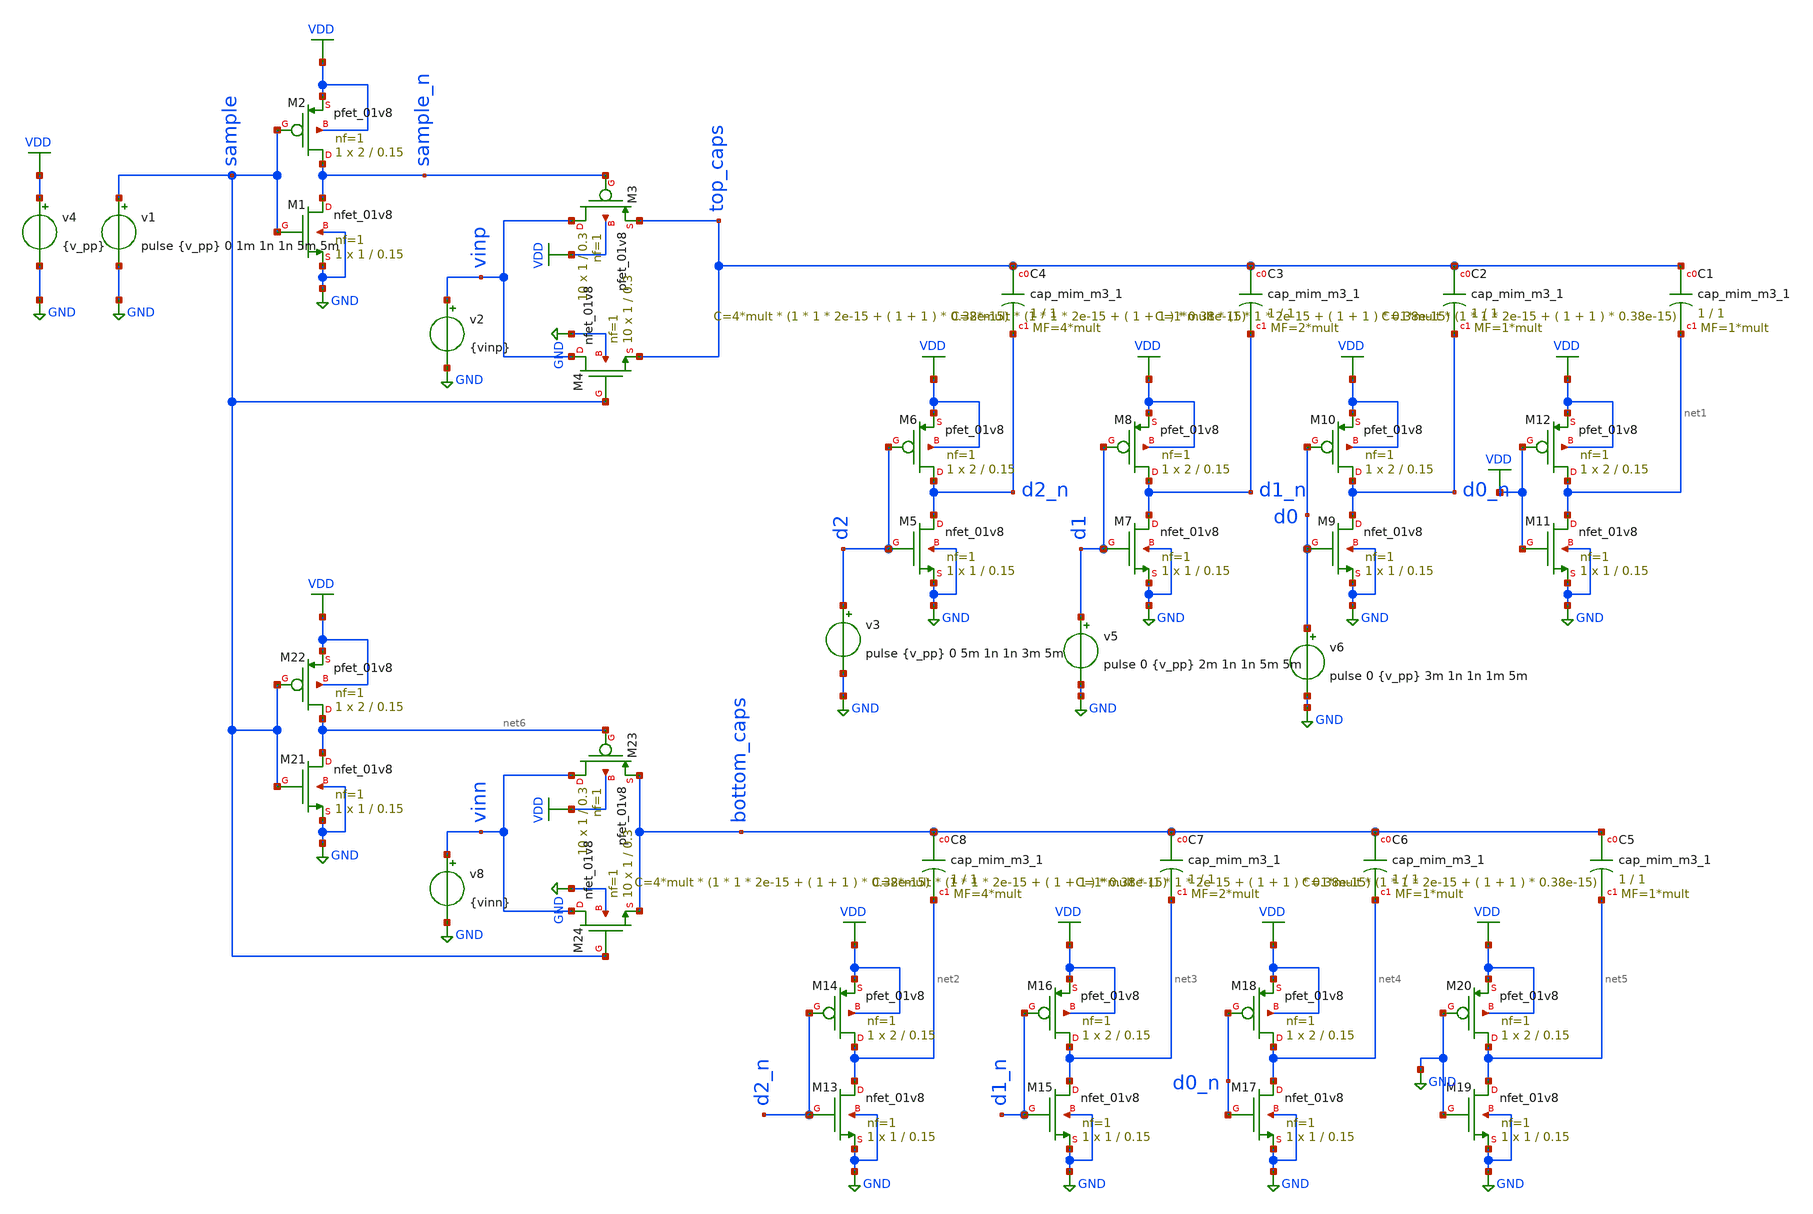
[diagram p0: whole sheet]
** sch_path: Schematics/ADC/simulations_adc_various/remake_c_transistors.sch
**.subckt remake_c_transistors
v1 sample GND pulse {v_pp} 0 1m 1n 1n 5m 5m
v4 VDD GND {v_pp}
XM1 sample_n sample GND GND sky130_fd_pr__nfet_01v8 L=0.15 W=1 nf=1 ad='int((nf+1)/2) * W/nf * 0.29'
+ as='int((nf+2)/2) * W/nf * 0.29' pd='2*int((nf+1)/2) * (W/nf + 0.29)' ps='2*int((nf+2)/2) * (W/nf + 0.29)'
+ nrd='0.29 / W' nrs='0.29 / W' sa=0 sb=0 sd=0 mult=1 m=1
XM2 sample_n sample VDD VDD sky130_fd_pr__pfet_01v8 L=0.15 W=2 nf=1 ad='int((nf+1)/2) * W/nf * 0.29'
+ as='int((nf+2)/2) * W/nf * 0.29' pd='2*int((nf+1)/2) * (W/nf + 0.29)' ps='2*int((nf+2)/2) * (W/nf + 0.29)'
+ nrd='0.29 / W' nrs='0.29 / W' sa=0 sb=0 sd=0 mult=1 m=1
XM3 vinp sample_n top_caps VDD sky130_fd_pr__pfet_01v8 L=0.3 W=1 nf=1 ad='int((nf+1)/2) * W/nf * 0.29'
+ as='int((nf+2)/2) * W/nf * 0.29' pd='2*int((nf+1)/2) * (W/nf + 0.29)' ps='2*int((nf+2)/2) * (W/nf + 0.29)'
+ nrd='0.29 / W' nrs='0.29 / W' sa=0 sb=0 sd=0 mult=10 m=10
XM4 vinp sample top_caps GND sky130_fd_pr__nfet_01v8 L=0.3 W=1 nf=1 ad='int((nf+1)/2) * W/nf * 0.29'
+ as='int((nf+2)/2) * W/nf * 0.29' pd='2*int((nf+1)/2) * (W/nf + 0.29)' ps='2*int((nf+2)/2) * (W/nf + 0.29)'
+ nrd='0.29 / W' nrs='0.29 / W' sa=0 sb=0 sd=0 mult=10 m=10
v2 vinp GND {vinp}
XM5 d2_n d2 GND GND sky130_fd_pr__nfet_01v8 L=0.15 W=1 nf=1 ad='int((nf+1)/2) * W/nf * 0.29' as='int((nf+2)/2) * W/nf * 0.29'
+ pd='2*int((nf+1)/2) * (W/nf + 0.29)' ps='2*int((nf+2)/2) * (W/nf + 0.29)' nrd='0.29 / W' nrs='0.29 / W'
+ sa=0 sb=0 sd=0 mult=1 m=1
XM6 d2_n d2 VDD VDD sky130_fd_pr__pfet_01v8 L=0.15 W=2 nf=1 ad='int((nf+1)/2) * W/nf * 0.29' as='int((nf+2)/2) * W/nf * 0.29'
+ pd='2*int((nf+1)/2) * (W/nf + 0.29)' ps='2*int((nf+2)/2) * (W/nf + 0.29)' nrd='0.29 / W' nrs='0.29 / W'
+ sa=0 sb=0 sd=0 mult=1 m=1
XM7 d1_n d1 GND GND sky130_fd_pr__nfet_01v8 L=0.15 W=1 nf=1 ad='int((nf+1)/2) * W/nf * 0.29' as='int((nf+2)/2) * W/nf * 0.29'
+ pd='2*int((nf+1)/2) * (W/nf + 0.29)' ps='2*int((nf+2)/2) * (W/nf + 0.29)' nrd='0.29 / W' nrs='0.29 / W'
+ sa=0 sb=0 sd=0 mult=1 m=1
XM8 d1_n d1 VDD VDD sky130_fd_pr__pfet_01v8 L=0.15 W=2 nf=1 ad='int((nf+1)/2) * W/nf * 0.29' as='int((nf+2)/2) * W/nf * 0.29'
+ pd='2*int((nf+1)/2) * (W/nf + 0.29)' ps='2*int((nf+2)/2) * (W/nf + 0.29)' nrd='0.29 / W' nrs='0.29 / W'
+ sa=0 sb=0 sd=0 mult=1 m=1
XM9 d0_n d0 GND GND sky130_fd_pr__nfet_01v8 L=0.15 W=1 nf=1 ad='int((nf+1)/2) * W/nf * 0.29' as='int((nf+2)/2) * W/nf * 0.29'
+ pd='2*int((nf+1)/2) * (W/nf + 0.29)' ps='2*int((nf+2)/2) * (W/nf + 0.29)' nrd='0.29 / W' nrs='0.29 / W'
+ sa=0 sb=0 sd=0 mult=1 m=1
XM10 d0_n d0 VDD VDD sky130_fd_pr__pfet_01v8 L=0.15 W=2 nf=1 ad='int((nf+1)/2) * W/nf * 0.29' as='int((nf+2)/2) * W/nf * 0.29'
+ pd='2*int((nf+1)/2) * (W/nf + 0.29)' ps='2*int((nf+2)/2) * (W/nf + 0.29)' nrd='0.29 / W' nrs='0.29 / W'
+ sa=0 sb=0 sd=0 mult=1 m=1
XM11 net1 VDD GND GND sky130_fd_pr__nfet_01v8 L=0.15 W=1 nf=1 ad='int((nf+1)/2) * W/nf * 0.29' as='int((nf+2)/2) * W/nf * 0.29'
+ pd='2*int((nf+1)/2) * (W/nf + 0.29)' ps='2*int((nf+2)/2) * (W/nf + 0.29)' nrd='0.29 / W' nrs='0.29 / W'
+ sa=0 sb=0 sd=0 mult=1 m=1
XM12 net1 VDD VDD VDD sky130_fd_pr__pfet_01v8 L=0.15 W=2 nf=1 ad='int((nf+1)/2) * W/nf * 0.29' as='int((nf+2)/2) * W/nf * 0.29'
+ pd='2*int((nf+1)/2) * (W/nf + 0.29)' ps='2*int((nf+2)/2) * (W/nf + 0.29)' nrd='0.29 / W' nrs='0.29 / W'
+ sa=0 sb=0 sd=0 mult=1 m=1
XC1 top_caps net1 sky130_fd_pr__cap_mim_m3_1 W=1 L=1 MF=1*mult m=1*mult
XC2 top_caps d0_n sky130_fd_pr__cap_mim_m3_1 W=1 L=1 MF=1*mult m=1*mult
XC3 top_caps d1_n sky130_fd_pr__cap_mim_m3_1 W=1 L=1 MF=2*mult m=2*mult
XC4 top_caps d2_n sky130_fd_pr__cap_mim_m3_1 W=1 L=1 MF=4*mult m=4*mult
v3 d2 GND pulse {v_pp} 0 5m 1n 1n 3m 5m
v5 d1 GND pulse 0 {v_pp} 2m 1n 1n 5m 5m
v6 d0 GND pulse 0 {v_pp} 3m 1n 1n 1m 5m
XM13 net2 d2_n GND GND sky130_fd_pr__nfet_01v8 L=0.15 W=1 nf=1 ad='int((nf+1)/2) * W/nf * 0.29' as='int((nf+2)/2) * W/nf * 0.29'
+ pd='2*int((nf+1)/2) * (W/nf + 0.29)' ps='2*int((nf+2)/2) * (W/nf + 0.29)' nrd='0.29 / W' nrs='0.29 / W'
+ sa=0 sb=0 sd=0 mult=1 m=1
XM14 net2 d2_n VDD VDD sky130_fd_pr__pfet_01v8 L=0.15 W=2 nf=1 ad='int((nf+1)/2) * W/nf * 0.29' as='int((nf+2)/2) * W/nf * 0.29'
+ pd='2*int((nf+1)/2) * (W/nf + 0.29)' ps='2*int((nf+2)/2) * (W/nf + 0.29)' nrd='0.29 / W' nrs='0.29 / W'
+ sa=0 sb=0 sd=0 mult=1 m=1
XM15 net3 d1_n GND GND sky130_fd_pr__nfet_01v8 L=0.15 W=1 nf=1 ad='int((nf+1)/2) * W/nf * 0.29' as='int((nf+2)/2) * W/nf * 0.29'
+ pd='2*int((nf+1)/2) * (W/nf + 0.29)' ps='2*int((nf+2)/2) * (W/nf + 0.29)' nrd='0.29 / W' nrs='0.29 / W'
+ sa=0 sb=0 sd=0 mult=1 m=1
XM16 net3 d1_n VDD VDD sky130_fd_pr__pfet_01v8 L=0.15 W=2 nf=1 ad='int((nf+1)/2) * W/nf * 0.29' as='int((nf+2)/2) * W/nf * 0.29'
+ pd='2*int((nf+1)/2) * (W/nf + 0.29)' ps='2*int((nf+2)/2) * (W/nf + 0.29)' nrd='0.29 / W' nrs='0.29 / W'
+ sa=0 sb=0 sd=0 mult=1 m=1
XM17 net4 d0_n GND GND sky130_fd_pr__nfet_01v8 L=0.15 W=1 nf=1 ad='int((nf+1)/2) * W/nf * 0.29' as='int((nf+2)/2) * W/nf * 0.29'
+ pd='2*int((nf+1)/2) * (W/nf + 0.29)' ps='2*int((nf+2)/2) * (W/nf + 0.29)' nrd='0.29 / W' nrs='0.29 / W'
+ sa=0 sb=0 sd=0 mult=1 m=1
XM18 net4 d0_n VDD VDD sky130_fd_pr__pfet_01v8 L=0.15 W=2 nf=1 ad='int((nf+1)/2) * W/nf * 0.29' as='int((nf+2)/2) * W/nf * 0.29'
+ pd='2*int((nf+1)/2) * (W/nf + 0.29)' ps='2*int((nf+2)/2) * (W/nf + 0.29)' nrd='0.29 / W' nrs='0.29 / W'
+ sa=0 sb=0 sd=0 mult=1 m=1
XM19 net5 GND GND GND sky130_fd_pr__nfet_01v8 L=0.15 W=1 nf=1 ad='int((nf+1)/2) * W/nf * 0.29' as='int((nf+2)/2) * W/nf * 0.29'
+ pd='2*int((nf+1)/2) * (W/nf + 0.29)' ps='2*int((nf+2)/2) * (W/nf + 0.29)' nrd='0.29 / W' nrs='0.29 / W'
+ sa=0 sb=0 sd=0 mult=1 m=1
XM20 net5 GND VDD VDD sky130_fd_pr__pfet_01v8 L=0.15 W=2 nf=1 ad='int((nf+1)/2) * W/nf * 0.29' as='int((nf+2)/2) * W/nf * 0.29'
+ pd='2*int((nf+1)/2) * (W/nf + 0.29)' ps='2*int((nf+2)/2) * (W/nf + 0.29)' nrd='0.29 / W' nrs='0.29 / W'
+ sa=0 sb=0 sd=0 mult=1 m=1
XC5 bottom_caps net5 sky130_fd_pr__cap_mim_m3_1 W=1 L=1 MF=1*mult m=1*mult
XC6 bottom_caps net4 sky130_fd_pr__cap_mim_m3_1 W=1 L=1 MF=1*mult m=1*mult
XC7 bottom_caps net3 sky130_fd_pr__cap_mim_m3_1 W=1 L=1 MF=2*mult m=2*mult
XC8 bottom_caps net2 sky130_fd_pr__cap_mim_m3_1 W=1 L=1 MF=4*mult m=4*mult
XM21 net6 sample GND GND sky130_fd_pr__nfet_01v8 L=0.15 W=1 nf=1 ad='int((nf+1)/2) * W/nf * 0.29' as='int((nf+2)/2) * W/nf * 0.29'
+ pd='2*int((nf+1)/2) * (W/nf + 0.29)' ps='2*int((nf+2)/2) * (W/nf + 0.29)' nrd='0.29 / W' nrs='0.29 / W'
+ sa=0 sb=0 sd=0 mult=1 m=1
XM22 net6 sample VDD VDD sky130_fd_pr__pfet_01v8 L=0.15 W=2 nf=1 ad='int((nf+1)/2) * W/nf * 0.29' as='int((nf+2)/2) * W/nf * 0.29'
+ pd='2*int((nf+1)/2) * (W/nf + 0.29)' ps='2*int((nf+2)/2) * (W/nf + 0.29)' nrd='0.29 / W' nrs='0.29 / W'
+ sa=0 sb=0 sd=0 mult=1 m=1
XM23 vinn net6 bottom_caps VDD sky130_fd_pr__pfet_01v8 L=0.3 W=1 nf=1 ad='int((nf+1)/2) * W/nf * 0.29'
+ as='int((nf+2)/2) * W/nf * 0.29' pd='2*int((nf+1)/2) * (W/nf + 0.29)' ps='2*int((nf+2)/2) * (W/nf + 0.29)'
+ nrd='0.29 / W' nrs='0.29 / W' sa=0 sb=0 sd=0 mult=10 m=10
XM24 vinn sample bottom_caps GND sky130_fd_pr__nfet_01v8 L=0.3 W=1 nf=1 ad='int((nf+1)/2) * W/nf * 0.29'
+ as='int((nf+2)/2) * W/nf * 0.29' pd='2*int((nf+1)/2) * (W/nf + 0.29)' ps='2*int((nf+2)/2) * (W/nf + 0.29)'
+ nrd='0.29 / W' nrs='0.29 / W' sa=0 sb=0 sd=0 mult=10 m=10
v8 vinn GND {vinn}
**** begin user architecture code

** opencircuitdesign pdks install
.lib $::SKYWATER_MODELS/sky130.lib.spice tt


**** end user architecture code
**.ends
.GLOBAL GND
.GLOBAL VDD
**** begin user architecture code

* .option SCALE=1e-6
.option method=gear seed=12
.control
.param mult=83
.param v_pp=1.8
.param vinp=1.46
.param vinn=v_pp-vinp
save all
tran 100n 5m
write remake_c.raw
set color0=white
set color1=black
set xbrushwidth=5
plot d0_n d1_n+4 d2_n+8 d0+12 d1+16 d2+20 sample+24
plot top_caps bottom_caps
.endc


**** end user architecture code
.end
